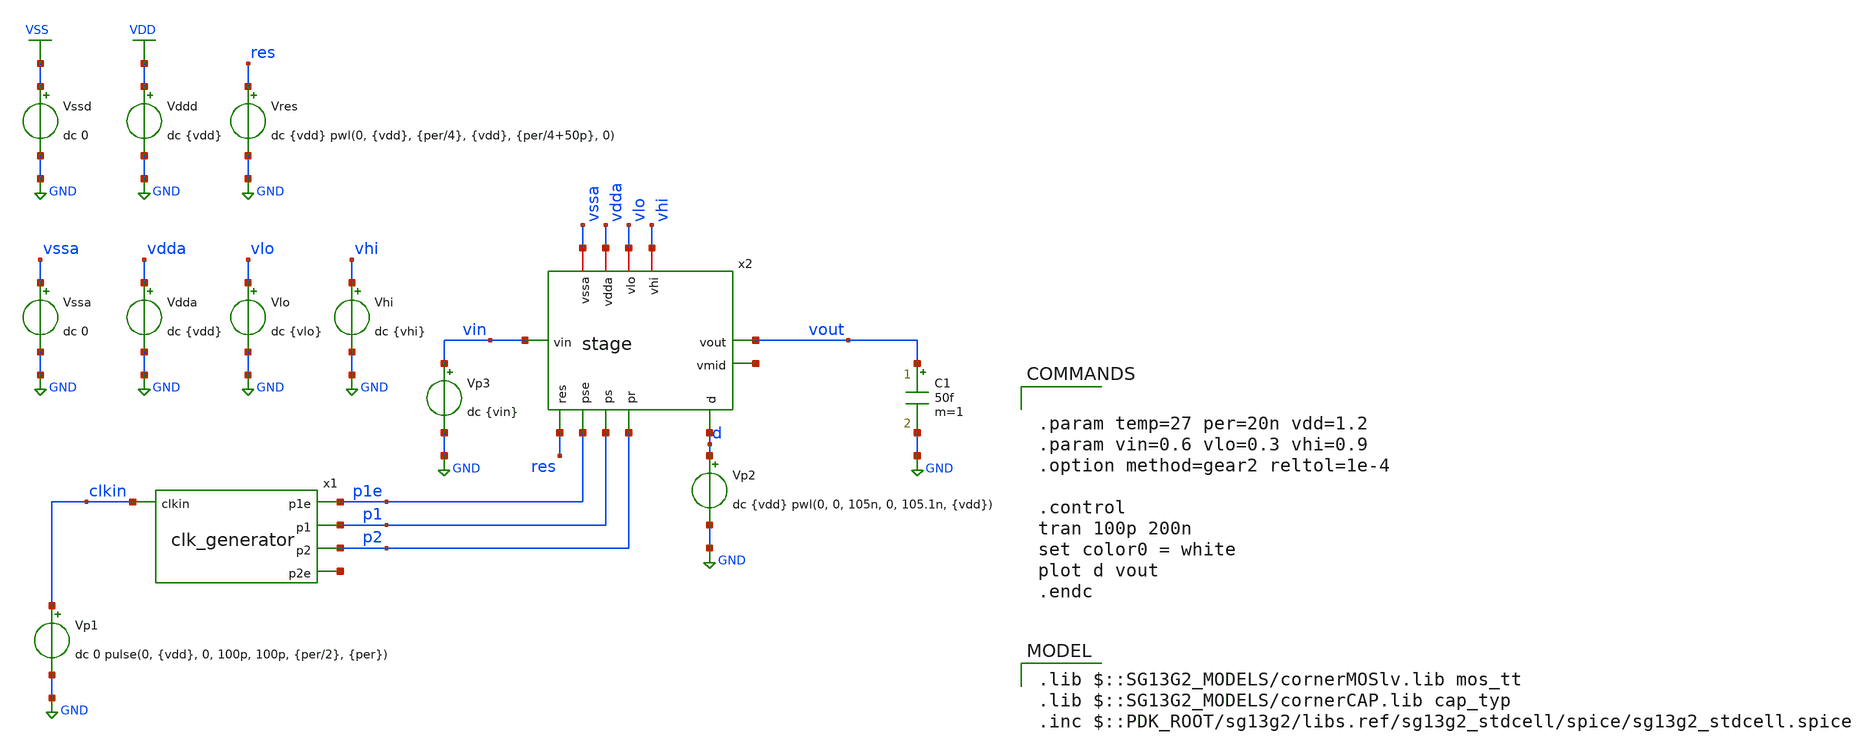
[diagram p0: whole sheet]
** sch_path: schematics/tb_stage.sch
**.subckt tb_stage
Vddd VDD GND dc {vdd}
Vssd VSS GND dc 0
Vp1 clkin GND dc 0 pulse(0, {vdd}, 0, 100p, 100p, {per/2}, {per})
C1 vout GND 50f m=1
x1 p1e clkin p1 p2 net1 clk_generator
x2 res p1e p1 p2 vin vout vssa d net2 vdda vhi vlo stage
Vp2 d GND dc {vdd} pwl(0, 0, 105n, 0, 105.1n, {vdd})
Vp3 vin GND dc {vin}
Vres res GND dc {vdd} pwl(0, {vdd}, {per/4}, {vdd}, {per/4+50p}, 0)
Vssa vssa GND dc 0
Vdda vdda GND dc {vdd}
Vlo vlo GND dc {vlo}
Vhi vhi GND dc {vhi}
**** begin user architecture code


.param temp=27 per=20n vdd=1.2
.param vin=0.6 vlo=0.3 vhi=0.9
.option method=gear2 reltol=1e-4

.control
tran 100p 200n
set color0 = white
plot d vout
.endc


 .lib $::SG13G2_MODELS/cornerMOSlv.lib mos_tt
.lib $::SG13G2_MODELS/cornerCAP.lib cap_typ
.inc $::PDK_ROOT/sg13g2/libs.ref/sg13g2_stdcell/spice/sg13g2_stdcell.spice

**** end user architecture code
**.ends
.GLOBAL VDD
.GLOBAL GND
.GLOBAL VSS
.end
